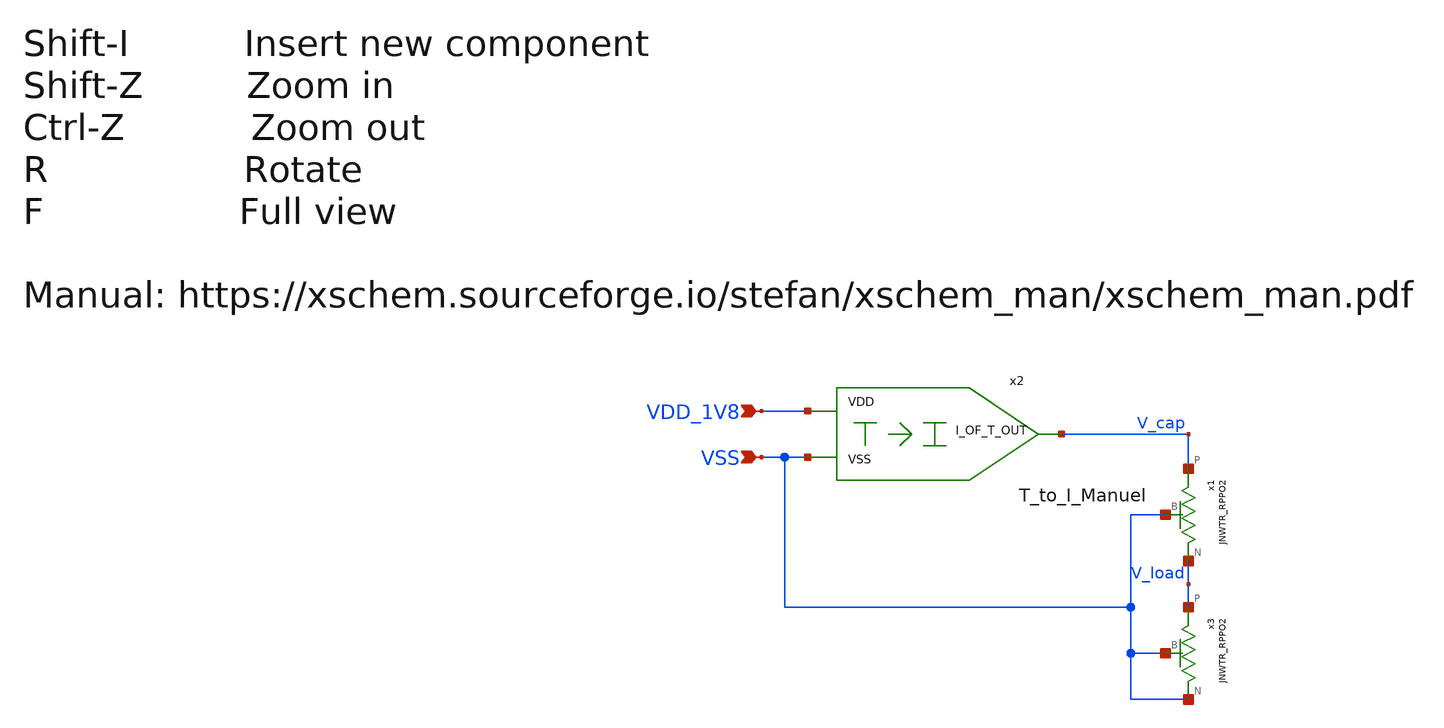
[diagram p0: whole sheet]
** sch_path: design/JNW_GR05_SKY130A/JNW_GR05.sch
**.subckt JNW_GR05 VDD_1V8 VSS
*.ipin VDD_1V8
*.ipin VSS
x2 VDD_1V8 V_cap VSS T_to_I_Manuel
x1 V_load V_cap VSS JNWTR_RPPO2
x3 VSS V_load VSS JNWTR_RPPO2
**.ends
.end
